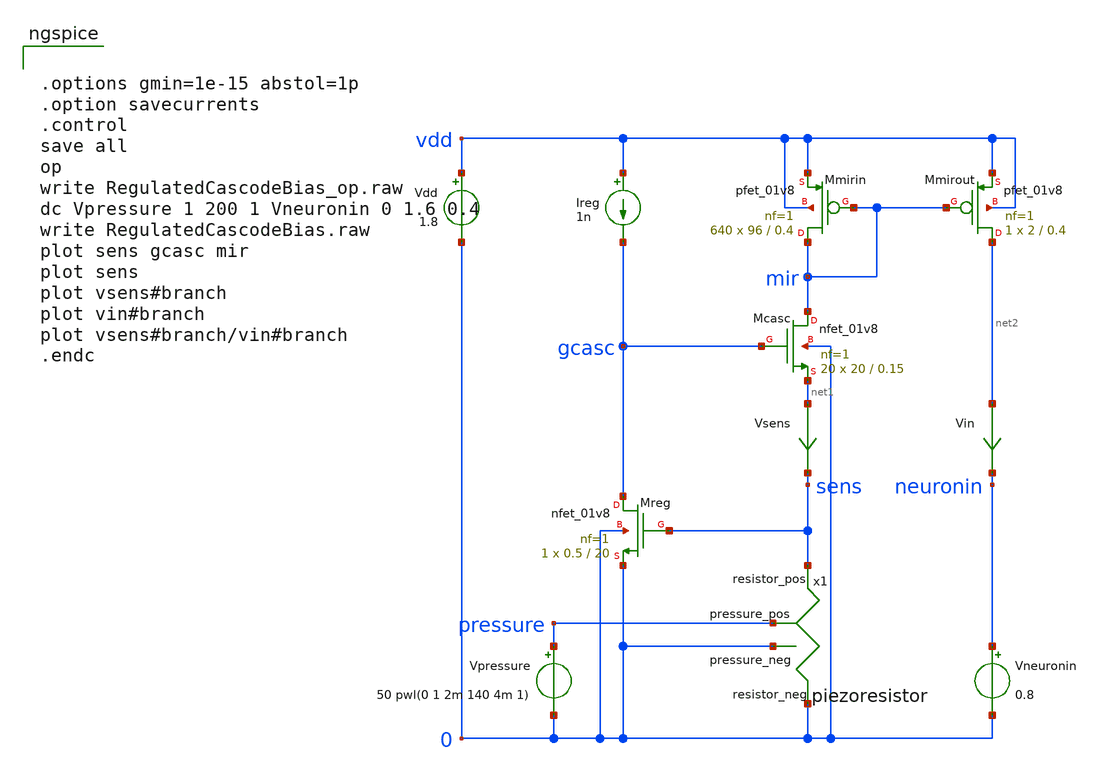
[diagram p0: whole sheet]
** sch_path: circuits/RegulatedCascodeBias.sch
* Copyright 2020 Stefan Frederik Schippers
* Licensed under the Apache License, Version 2.0 (the "License");
* you may not use this file except in compliance with the License.
* You may obtain a copy of the License at
* https://www.apache.org/licenses/LICENSE-2.0
* Unless required by applicable law or agreed to in writing, software
* distributed under the License is distributed on an "AS IS" BASIS,
* WITHOUT WARRANTIES OR CONDITIONS OF ANY KIND, either express or implied.
* See the License for the specific language governing permissions and
* limitations under the License.
**.subckt RegulatedCascodeBias
Vdd vdd 0 1.8
Ireg vdd gcasc 1n
Vsens net1 sens 0
.save i(vsens)
XMmirout net2 mir vdd vdd sky130_fd_pr__pfet_01v8 L=0.4 W=2 nf=1 ad='int((nf+1)/2) * W/nf * 0.29' as='int((nf+2)/2) * W/nf * 0.29'
+ pd='2*int((nf+1)/2) * (W/nf + 0.29)' ps='2*int((nf+2)/2) * (W/nf + 0.29)' nrd='0.29 / W' nrs='0.29 / W'
+ sa=0 sb=0 sd=0 mult=1 m=1
XMmirin mir mir vdd vdd sky130_fd_pr__pfet_01v8 L=0.4 W=96 nf=1 ad='int((nf+1)/2) * W/nf * 0.29' as='int((nf+2)/2) * W/nf * 0.29'
+ pd='2*int((nf+1)/2) * (W/nf + 0.29)' ps='2*int((nf+2)/2) * (W/nf + 0.29)' nrd='0.29 / W' nrs='0.29 / W'
+ sa=0 sb=0 sd=0 mult=640 m=640
XMcasc mir gcasc net1 0 sky130_fd_pr__nfet_01v8 L=0.15 W=20 nf=1 ad='int((1 + 1)/2) * 20 / 1 * 0.29'
+ as='int((1 + 2)/2) * 20 / 1 * 0.29' pd='2*int((1 + 1)/2) * (20 / 1 + 0.29)' ps='2*int((1 + 2)/2) * (20 / 1 + 0.29)'
+ nrd='0.29 / 20 ' nrs='0.29 / 20 ' sa=0 sb=0 sd=0 mult=20 m=20
XMreg gcasc sens 0 0 sky130_fd_pr__nfet_01v8 L=20 W=0.5 nf=1 ad='int((1 + 1)/2) * 0.5 / 1 * 0.29' as='int((1 + 2)/2) * 0.5 / 1 * 0.29'
+ pd='2*int((1 + 1)/2) * (0.5 / 1 + 0.29)' ps='2*int((1 + 2)/2) * (0.5 / 1 + 0.29)' nrd='0.29 / 0.5 ' nrs='0.29 / 0.5 '
+ sa=0 sb=0 sd=0 mult=1 m=1
Vin net2 neuronin 0
.save i(vin)
x1 pressure 0 sens 0 piezoresistor
Vpressure pressure 0 50 pwl(0 1 2m 140 4m 1)
Vneuronin neuronin 0 0.8
**** begin user architecture code


.options gmin=1e-15 abstol=1p
.option savecurrents
.control
save all
op
write RegulatedCascodeBias_op.raw
dc Vpressure 1 200 1 Vneuronin 0 1.6 0.4
write RegulatedCascodeBias.raw
plot sens gcasc mir
plot sens
plot vsens#branch
plot vin#branch
plot vsens#branch/vin#branch
.endc


 .lib $::SKYWATER_MODELS/models/sky130.lib.spice tt

.param mc_mm_switch=0
.param mc_pr_switch=1


**** end user architecture code
**.ends

* expanding   symbol:  /home/cmaier/.xschem/sky130_TAC3/circuits/piezoresistor.sym # of pins=4
** sym_path: circuits/piezoresistor.sym
** sch_path: circuits/piezoresistor.sch
.subckt piezoresistor pressure_pos pressure_neg resistor_pos resistor_neg
*.ipin pressure_pos
*.ipin pressure_neg
*.iopin resistor_pos
*.iopin resistor_neg
Broot sqrtp 0 V = sqrt(v(pressure_pos,pressure_neg))
Bres res 0 V = 106*(50/v(sqrtp)-1)*exp(-0.328*v(sqrtp))+15
Brvar resistor_pos resistor_neg I = V(resistor_pos,resistor_neg)/V(res)
.ends

.end
